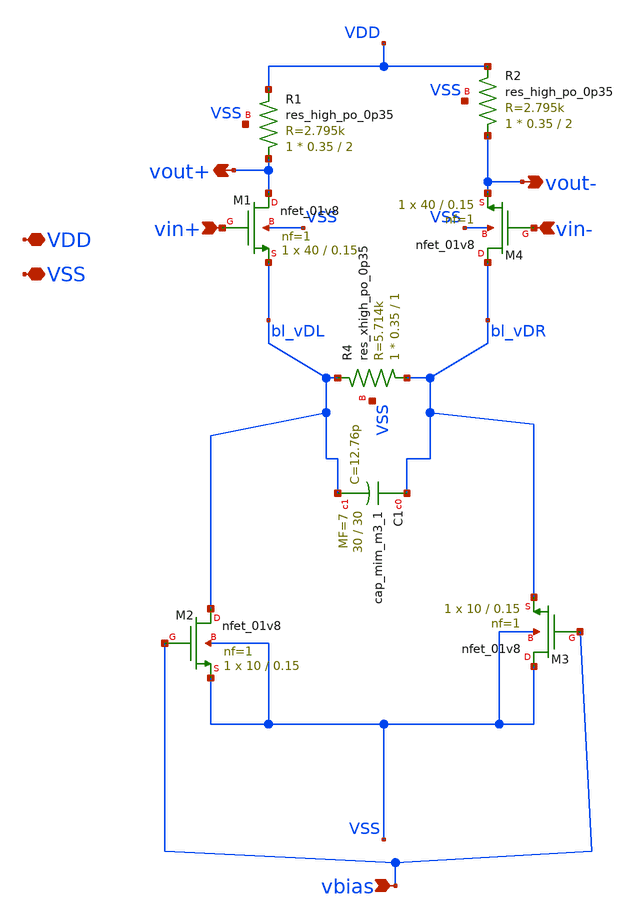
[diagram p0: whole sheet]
** sch_path: xschem/CTLE.sch
**.subckt CTLE VDD VSS vin+ vin- vout- vout+ vbias
*.iopin VDD
*.iopin VSS
*.ipin vin+
*.ipin vin-
*.opin vout-
*.opin vout+
*.ipin vbias
XR4 bl_vDR bl_vDL VSS sky130_fd_pr__res_xhigh_po_0p35 L=1 mult=1 m=1
XR1 vout+ VDD VSS sky130_fd_pr__res_high_po_0p35 L=2 mult=1 m=1
XR2 vout- VDD VSS sky130_fd_pr__res_high_po_0p35 L=2 mult=1 m=1
XC1 bl_vDR bl_vDL sky130_fd_pr__cap_mim_m3_1 W=30 L=30 MF=7 m=7
XM1 vout+ vin+ bl_vDL VSS sky130_fd_pr__nfet_01v8 L=0.15 W=40 nf=1 ad='int((nf+1)/2) * W/nf * 0.29' as='int((nf+2)/2) * W/nf * 0.29'
+ pd='2*int((nf+1)/2) * (W/nf + 0.29)' ps='2*int((nf+2)/2) * (W/nf + 0.29)' nrd='0.29 / W' nrs='0.29 / W'
+ sa=0 sb=0 sd=0 mult=1 m=1
XM4 bl_vDR vin- vout- VSS sky130_fd_pr__nfet_01v8 L=0.15 W=40 nf=1 ad='int((nf+1)/2) * W/nf * 0.29' as='int((nf+2)/2) * W/nf * 0.29'
+ pd='2*int((nf+1)/2) * (W/nf + 0.29)' ps='2*int((nf+2)/2) * (W/nf + 0.29)' nrd='0.29 / W' nrs='0.29 / W'
+ sa=0 sb=0 sd=0 mult=1 m=1
XM2 bl_vDL vbias VSS VSS sky130_fd_pr__nfet_01v8 L=0.15 W=10 nf=1 ad='int((nf+1)/2) * W/nf * 0.29' as='int((nf+2)/2) * W/nf * 0.29'
+ pd='2*int((nf+1)/2) * (W/nf + 0.29)' ps='2*int((nf+2)/2) * (W/nf + 0.29)' nrd='0.29 / W' nrs='0.29 / W'
+ sa=0 sb=0 sd=0 mult=1 m=1
XM3 VSS vbias bl_vDR VSS sky130_fd_pr__nfet_01v8 L=0.15 W=10 nf=1 ad='int((nf+1)/2) * W/nf * 0.29' as='int((nf+2)/2) * W/nf * 0.29'
+ pd='2*int((nf+1)/2) * (W/nf + 0.29)' ps='2*int((nf+2)/2) * (W/nf + 0.29)' nrd='0.29 / W' nrs='0.29 / W'
+ sa=0 sb=0 sd=0 mult=1 m=1
**.ends
.end
